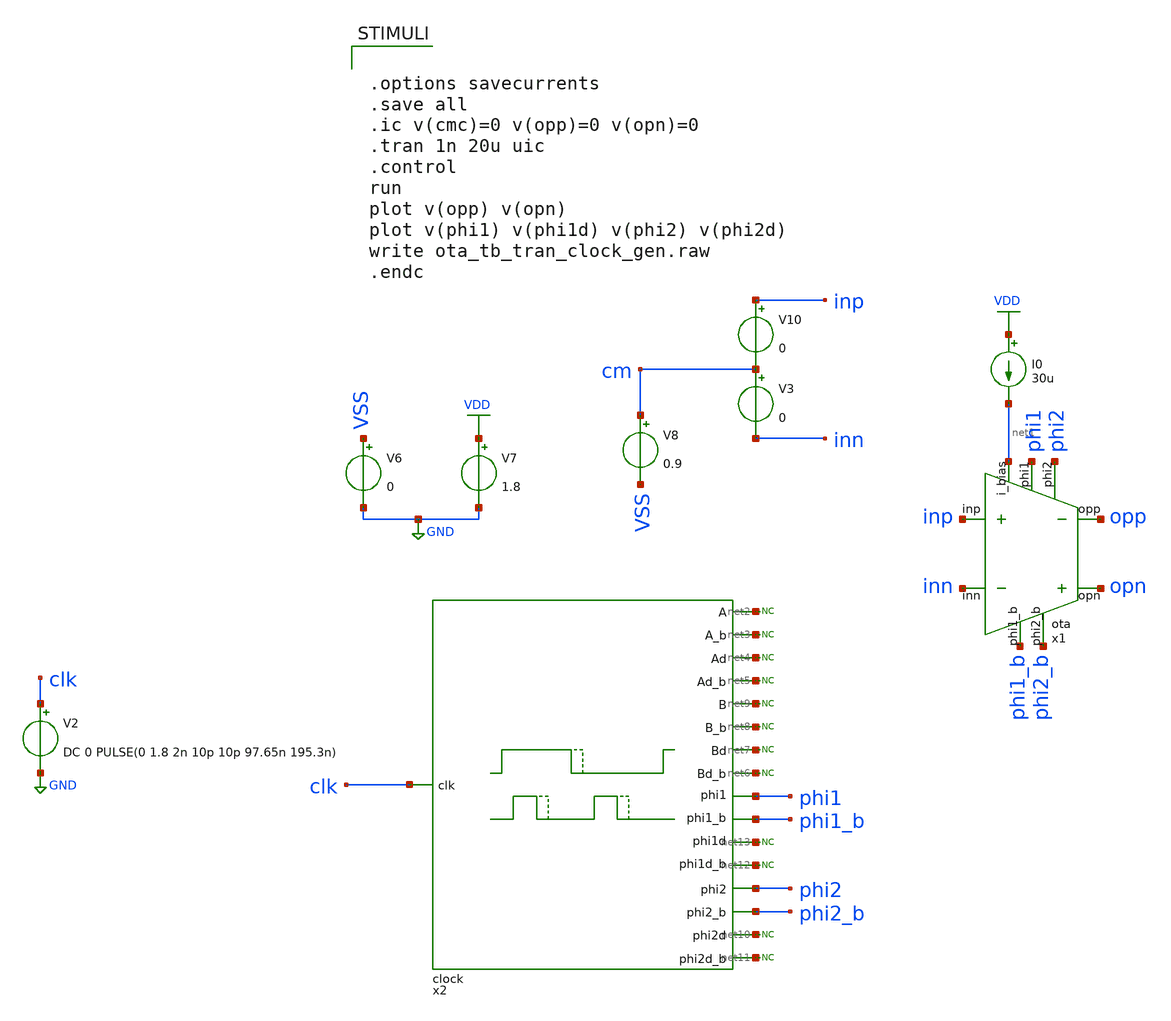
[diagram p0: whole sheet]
** sch_path: verification/analog_modulator/ota_tb_tran_clock_gen.sch
**.subckt ota_tb_tran_clock_gen
V6 VSS GND 0
V7 VDD GND 1.8
V8 cm VSS 0.9
V10 inp cm 0
V3 cm inn 0
I0 VDD net1 30u
V2 clk GND DC 0 PULSE(0 1.8 2n 10p 10p 97.65n 195.3n)
x2 net2 net3 net4 net5 net6 net7 net8 net9 phi2 phi2_b net10 clk net11 net12 net13 phi1_b phi1 VDD
+ VSS clock
x1 net1 inp inn phi1 phi1_b phi2 phi2_b opp opn 50 350 VDD VSS ota
* noconn #net2
* noconn #net3
* noconn #net4
* noconn #net5
* noconn #net9
* noconn #net8
* noconn #net7
* noconn #net6
* noconn #net13
* noconn #net12
* noconn #net10
* noconn #net11
**** begin user architecture code

** opencircuitdesign pdks install
.lib /farmshare/home/classes/ee/372/PDKs/open_pdks_1.0.310/sky130/sky130A/libs.tech/ngspice/sky130.lib.spice tt
.include /farmshare/home/classes/ee/372/PDKs/open_pdks_1.0.310/sky130/sky130A/libs.ref/sky130_fd_sc_hd/spice/sky130_fd_sc_hd.spice



.options savecurrents
.save all
.ic v(cmc)=0 v(opp)=0 v(opn)=0
.tran 1n 20u uic
.control
run
plot v(opp) v(opn)
plot v(phi1) v(phi1d) v(phi2) v(phi2d)
write ota_tb_tran_clock_gen.raw
.endc


**** end user architecture code
**.ends
.GLOBAL VDD
.GLOBAL GND
.end
